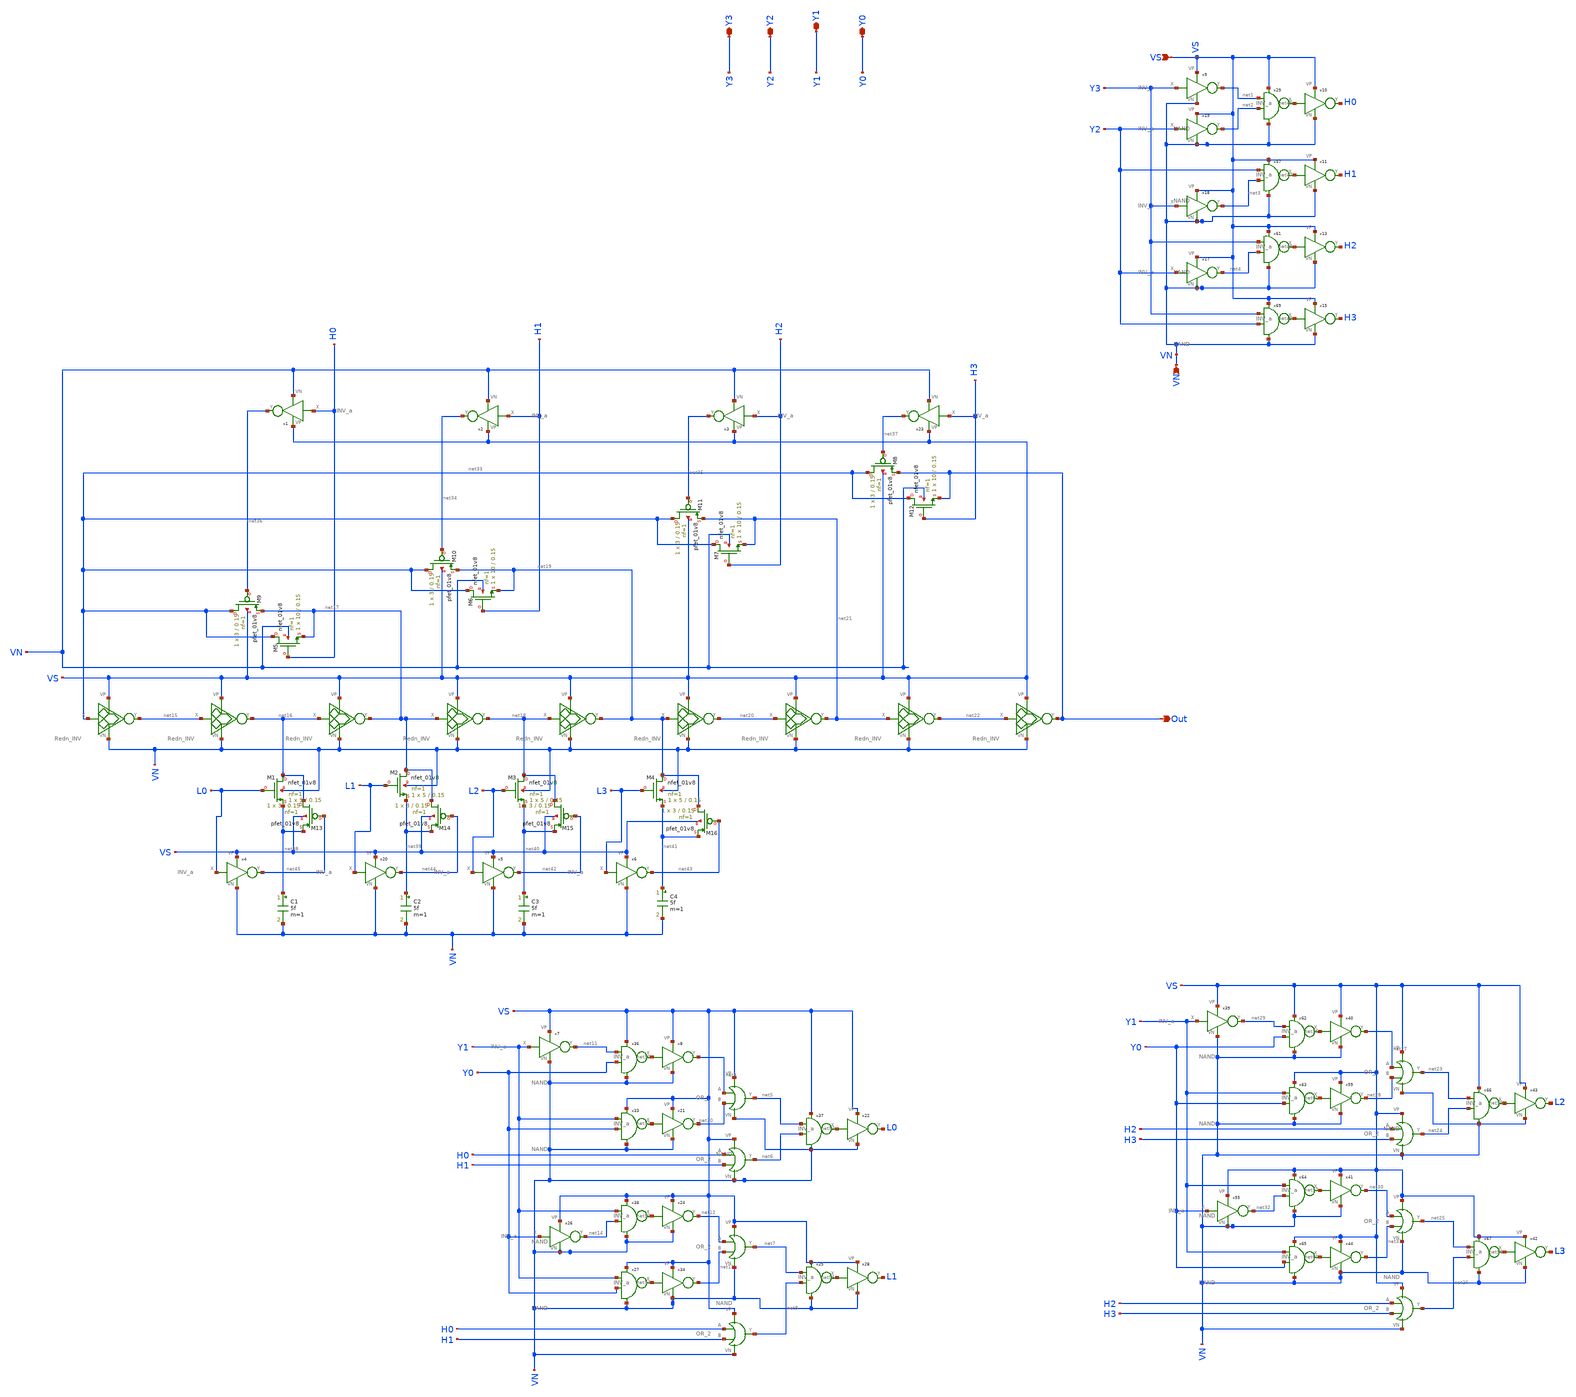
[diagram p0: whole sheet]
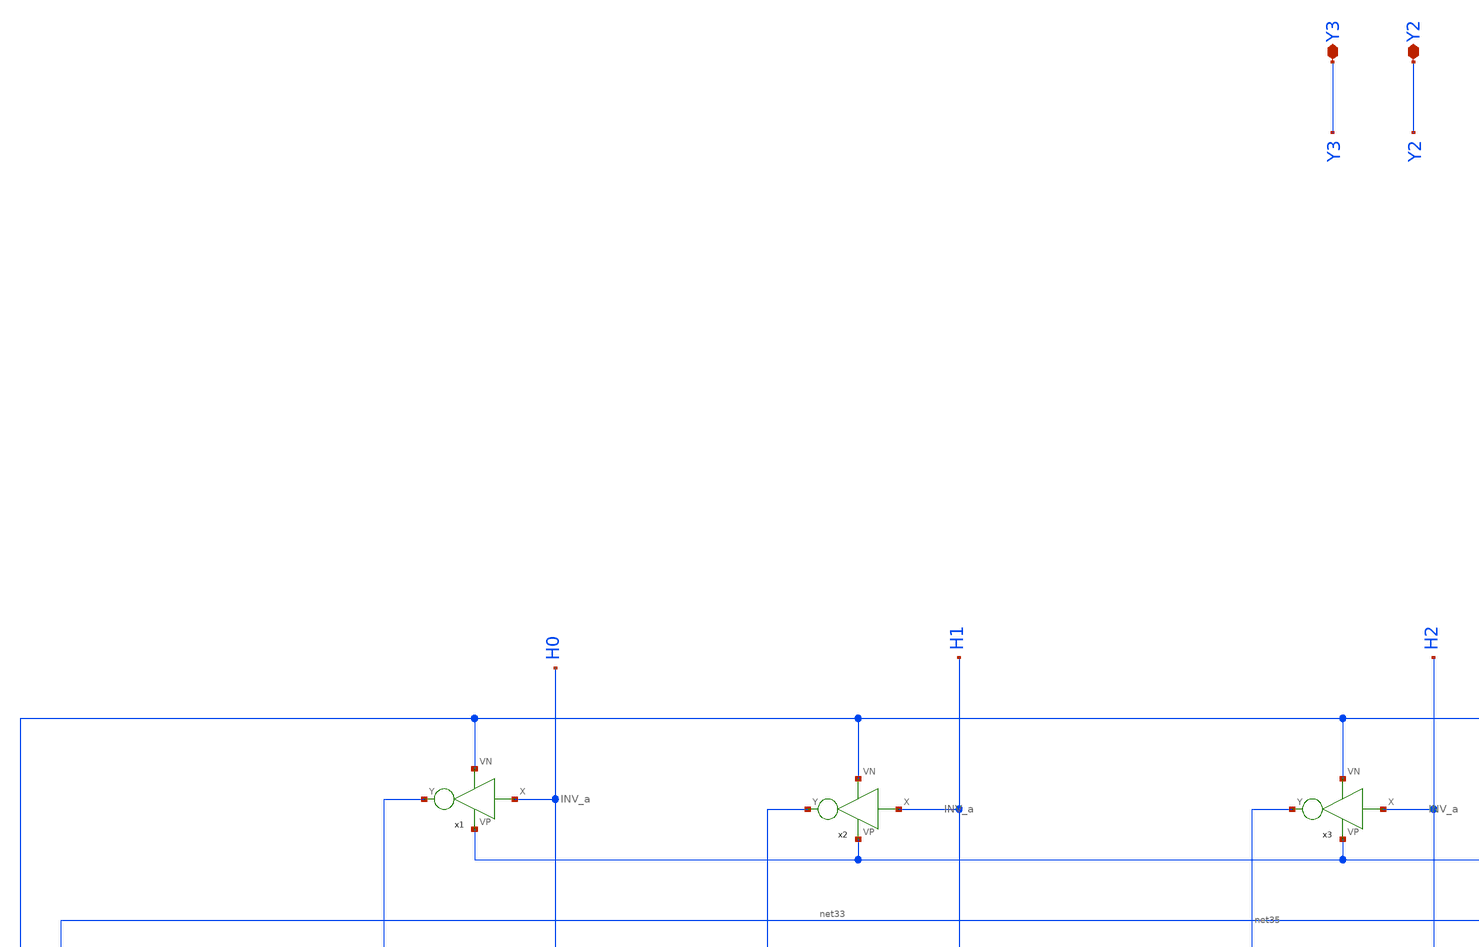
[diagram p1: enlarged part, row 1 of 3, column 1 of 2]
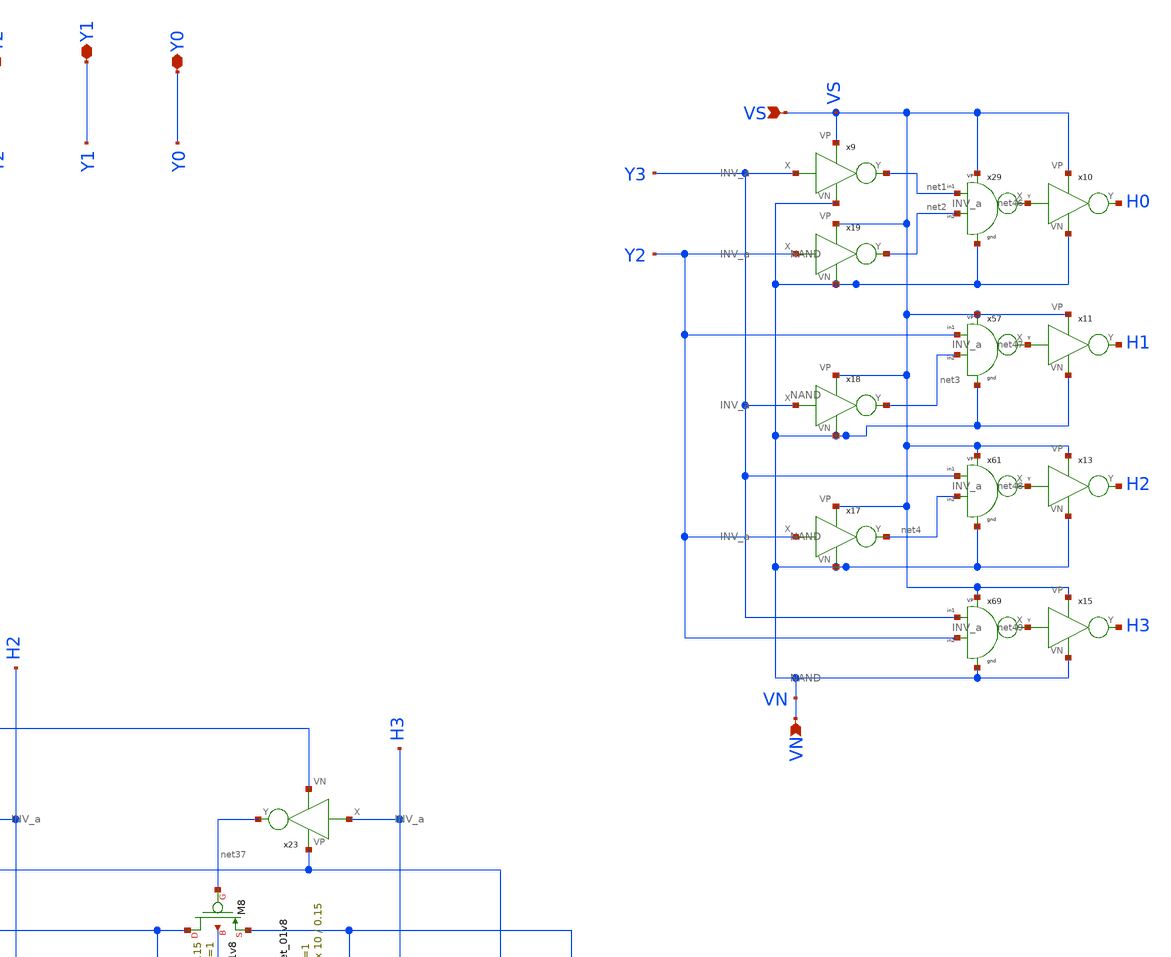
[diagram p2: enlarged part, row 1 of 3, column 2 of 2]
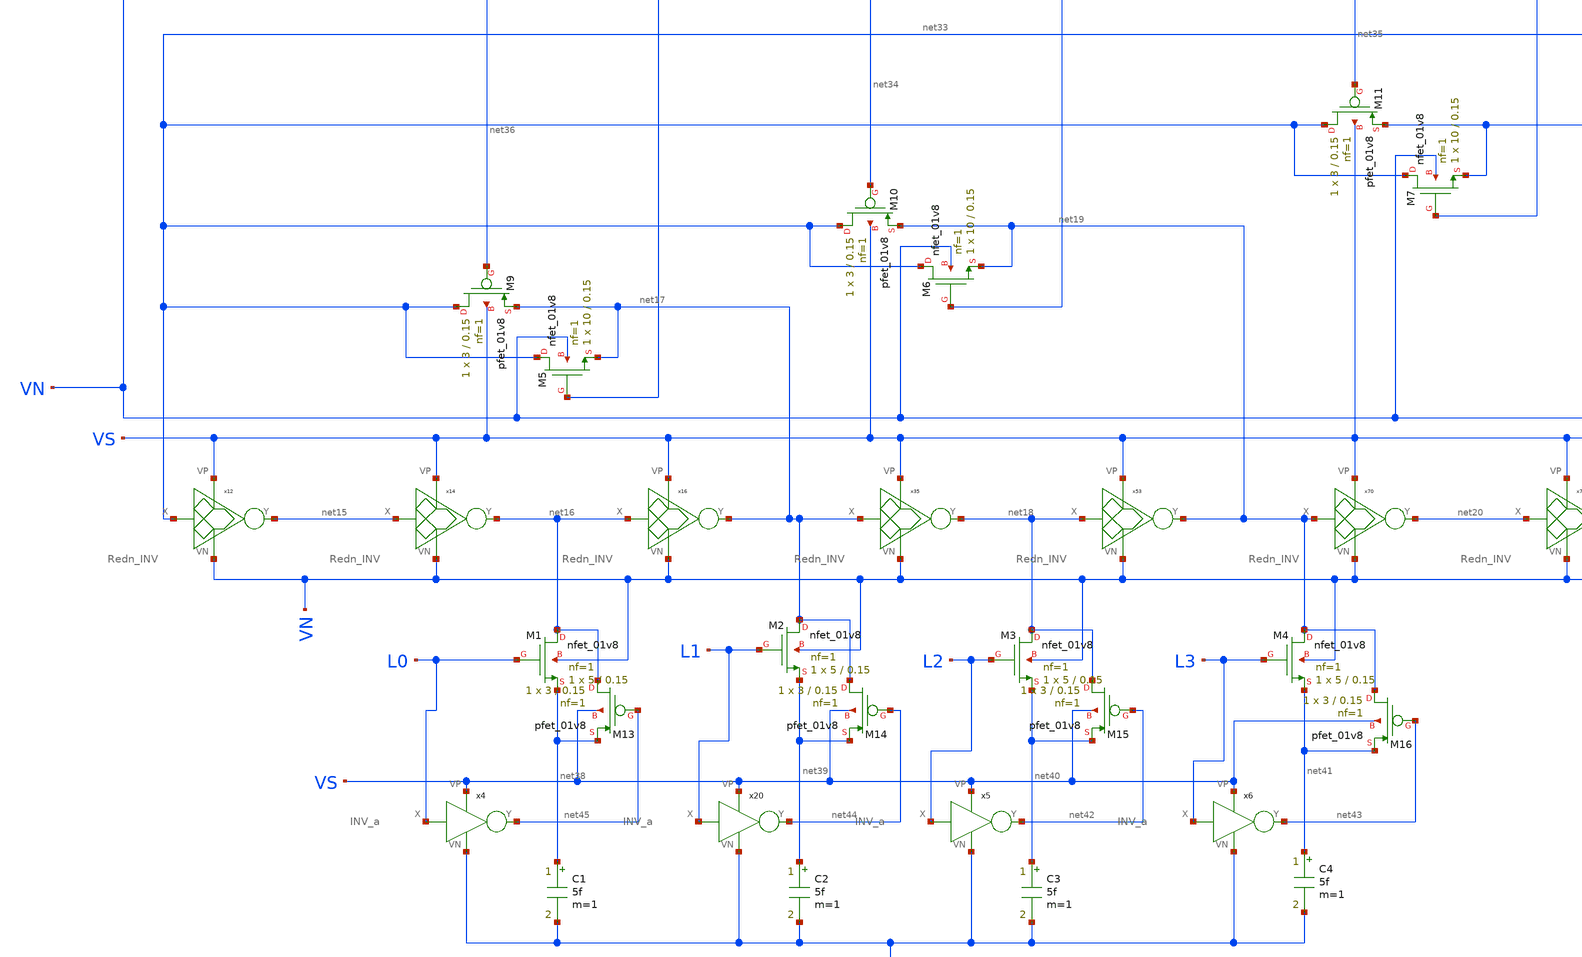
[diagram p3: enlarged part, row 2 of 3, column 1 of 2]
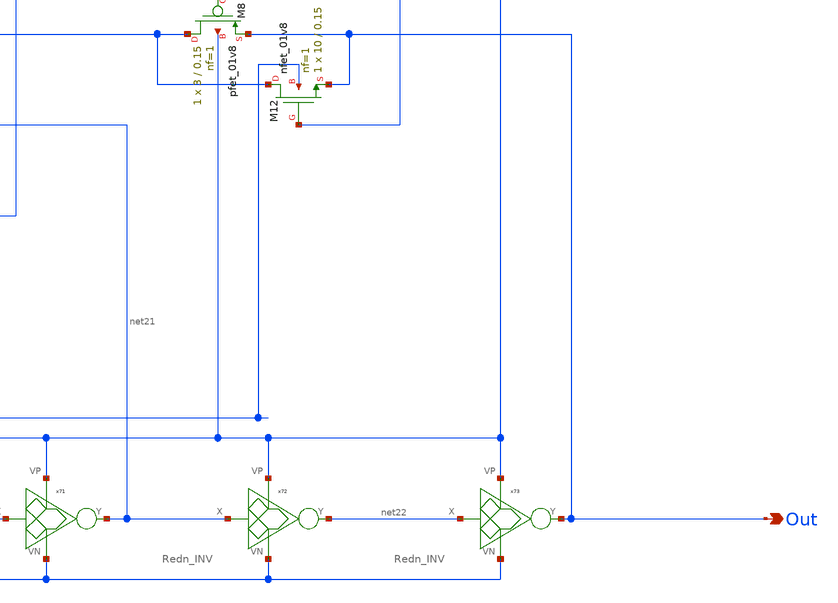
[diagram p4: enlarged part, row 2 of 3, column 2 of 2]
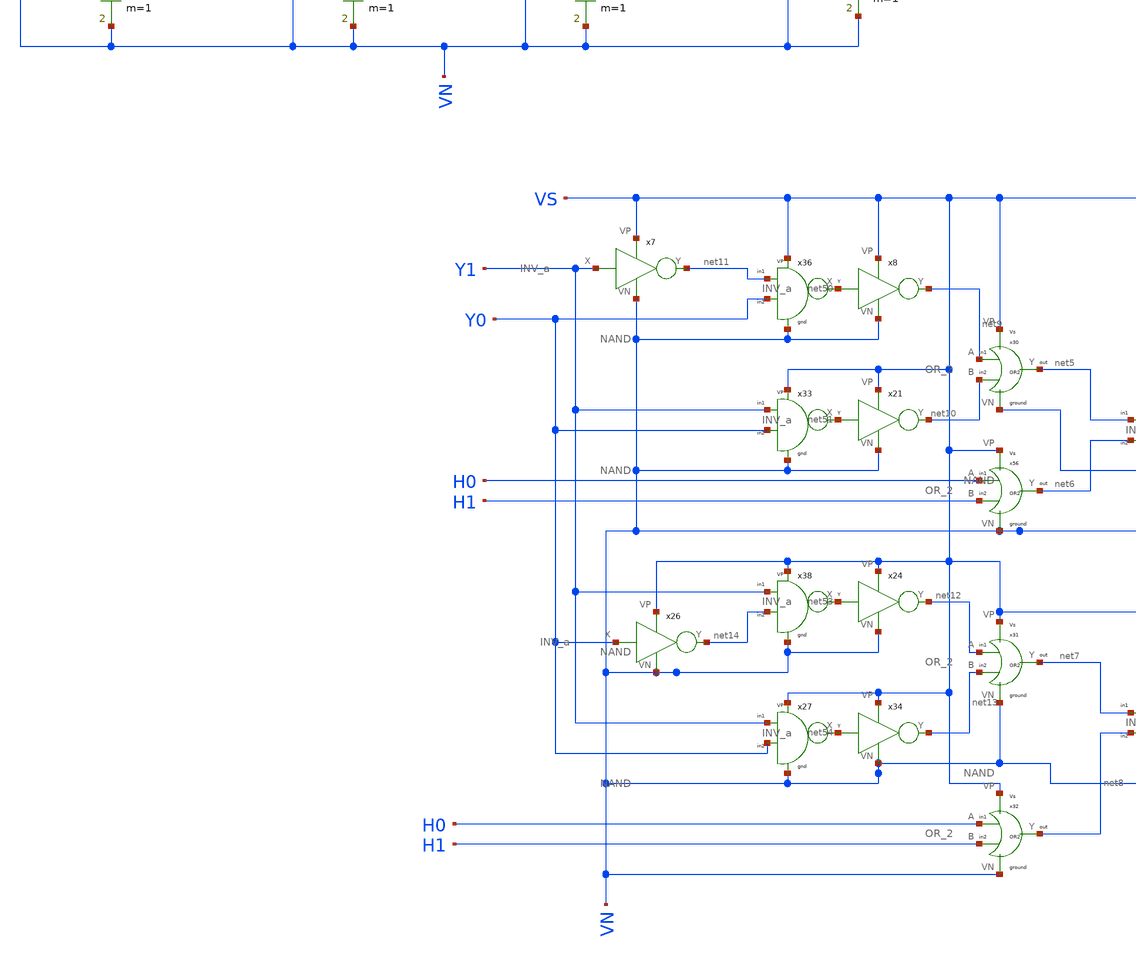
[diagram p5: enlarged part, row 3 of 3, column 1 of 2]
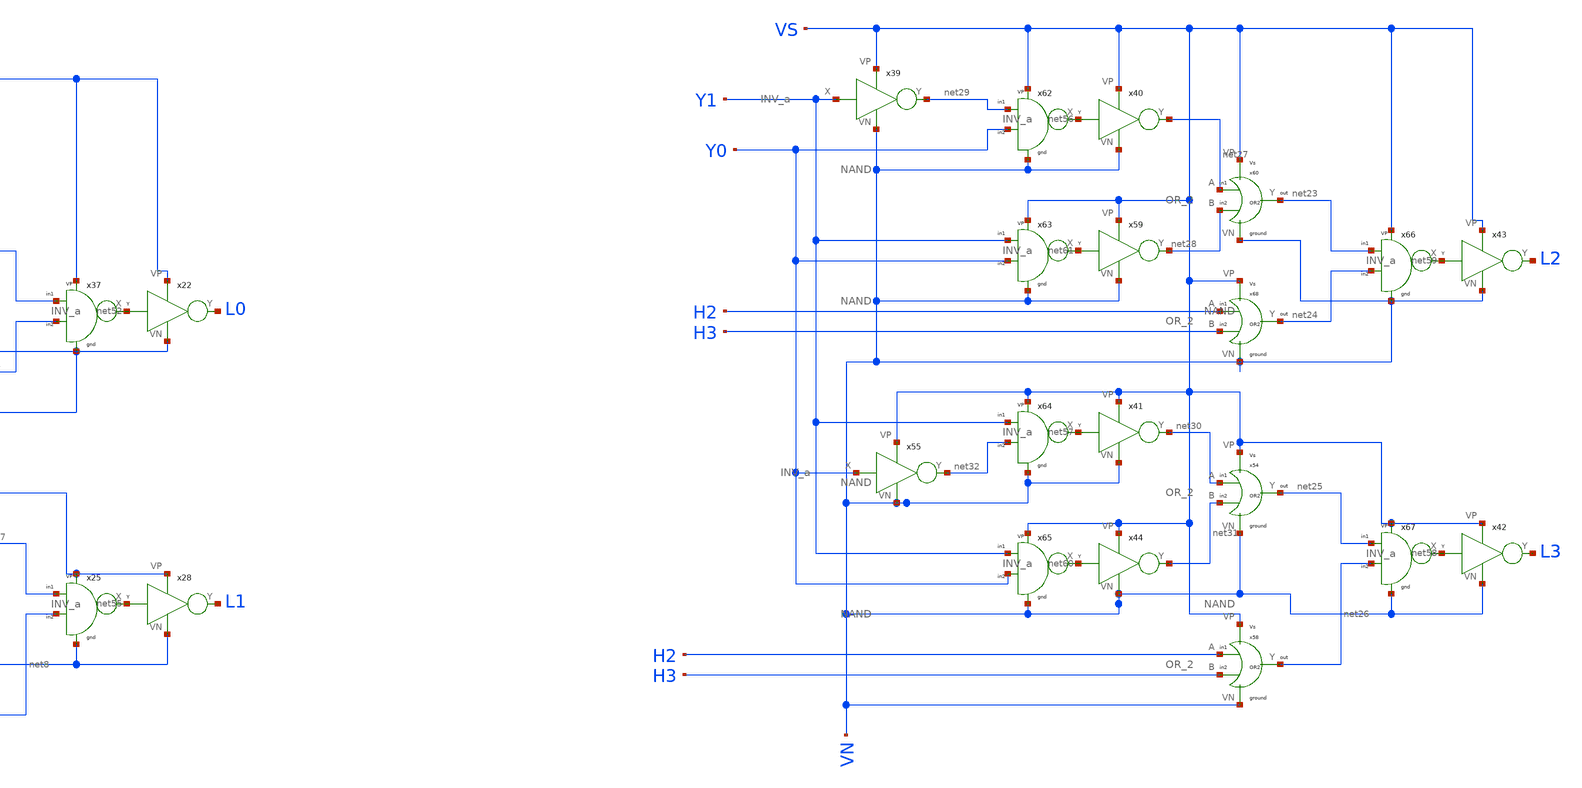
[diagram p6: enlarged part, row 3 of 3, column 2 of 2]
** sch_path: Blocks/DCO/DCO.sch
**.subckt DCO VS Out VN Y3 Y2 Y1 Y0
*.ipin VS
*.opin Out
*.ipin VN
*.iopin Y3
*.iopin Y2
*.iopin Y1
*.iopin Y0
C1 net38 VN 5f m=1
C2 net39 VN 5f m=1
C3 net40 VN 5f m=1
C4 net41 VN 5f m=1
XM1 net16 L0 net38 VN sky130_fd_pr__nfet_01v8 L=0.15 W=5 nf=1 ad='int((nf+1)/2) * W/nf * 0.29' as='int((nf+2)/2) * W/nf * 0.29'
+ pd='2*int((nf+1)/2) * (W/nf + 0.29)' ps='2*int((nf+2)/2) * (W/nf + 0.29)' nrd='0.29 / W' nrs='0.29 / W'
+ sa=0 sb=0 sd=0 mult=1 m=1
XM2 net17 L1 net39 VN sky130_fd_pr__nfet_01v8 L=0.15 W=5 nf=1 ad='int((nf+1)/2) * W/nf * 0.29' as='int((nf+2)/2) * W/nf * 0.29'
+ pd='2*int((nf+1)/2) * (W/nf + 0.29)' ps='2*int((nf+2)/2) * (W/nf + 0.29)' nrd='0.29 / W' nrs='0.29 / W'
+ sa=0 sb=0 sd=0 mult=1 m=1
XM3 net18 L2 net40 VN sky130_fd_pr__nfet_01v8 L=0.15 W=5 nf=1 ad='int((nf+1)/2) * W/nf * 0.29' as='int((nf+2)/2) * W/nf * 0.29'
+ pd='2*int((nf+1)/2) * (W/nf + 0.29)' ps='2*int((nf+2)/2) * (W/nf + 0.29)' nrd='0.29 / W' nrs='0.29 / W'
+ sa=0 sb=0 sd=0 mult=1 m=1
XM4 net19 L3 net41 VN sky130_fd_pr__nfet_01v8 L=0.15 W=5 nf=1 ad='int((nf+1)/2) * W/nf * 0.29' as='int((nf+2)/2) * W/nf * 0.29'
+ pd='2*int((nf+1)/2) * (W/nf + 0.29)' ps='2*int((nf+2)/2) * (W/nf + 0.29)' nrd='0.29 / W' nrs='0.29 / W'
+ sa=0 sb=0 sd=0 mult=1 m=1
XM5 net33 H0 net17 VN sky130_fd_pr__nfet_01v8 L=0.15 W=10 nf=1 ad='int((nf+1)/2) * W/nf * 0.29' as='int((nf+2)/2) * W/nf * 0.29'
+ pd='2*int((nf+1)/2) * (W/nf + 0.29)' ps='2*int((nf+2)/2) * (W/nf + 0.29)' nrd='0.29 / W' nrs='0.29 / W'
+ sa=0 sb=0 sd=0 mult=1 m=1
XM6 net33 H1 net19 VN sky130_fd_pr__nfet_01v8 L=0.15 W=10 nf=1 ad='int((nf+1)/2) * W/nf * 0.29' as='int((nf+2)/2) * W/nf * 0.29'
+ pd='2*int((nf+1)/2) * (W/nf + 0.29)' ps='2*int((nf+2)/2) * (W/nf + 0.29)' nrd='0.29 / W' nrs='0.29 / W'
+ sa=0 sb=0 sd=0 mult=1 m=1
XM7 net33 H2 net21 VN sky130_fd_pr__nfet_01v8 L=0.15 W=10 nf=1 ad='int((nf+1)/2) * W/nf * 0.29' as='int((nf+2)/2) * W/nf * 0.29'
+ pd='2*int((nf+1)/2) * (W/nf + 0.29)' ps='2*int((nf+2)/2) * (W/nf + 0.29)' nrd='0.29 / W' nrs='0.29 / W'
+ sa=0 sb=0 sd=0 mult=1 m=1
XM9 net33 net36 net17 VS sky130_fd_pr__pfet_01v8 L=0.15 W=3 nf=1 ad='int((nf+1)/2) * W/nf * 0.29' as='int((nf+2)/2) * W/nf * 0.29'
+ pd='2*int((nf+1)/2) * (W/nf + 0.29)' ps='2*int((nf+2)/2) * (W/nf + 0.29)' nrd='0.29 / W' nrs='0.29 / W'
+ sa=0 sb=0 sd=0 mult=1 m=1
XM10 net33 net34 net19 VS sky130_fd_pr__pfet_01v8 L=0.15 W=3 nf=1 ad='int((nf+1)/2) * W/nf * 0.29' as='int((nf+2)/2) * W/nf * 0.29'
+ pd='2*int((nf+1)/2) * (W/nf + 0.29)' ps='2*int((nf+2)/2) * (W/nf + 0.29)' nrd='0.29 / W' nrs='0.29 / W'
+ sa=0 sb=0 sd=0 mult=1 m=1
XM11 net33 net35 net21 VS sky130_fd_pr__pfet_01v8 L=0.15 W=3 nf=1 ad='int((nf+1)/2) * W/nf * 0.29' as='int((nf+2)/2) * W/nf * 0.29'
+ pd='2*int((nf+1)/2) * (W/nf + 0.29)' ps='2*int((nf+2)/2) * (W/nf + 0.29)' nrd='0.29 / W' nrs='0.29 / W'
+ sa=0 sb=0 sd=0 mult=1 m=1
XM8 net33 net37 Out VS sky130_fd_pr__pfet_01v8 L=0.15 W=3 nf=1 ad='int((nf+1)/2) * W/nf * 0.29' as='int((nf+2)/2) * W/nf * 0.29'
+ pd='2*int((nf+1)/2) * (W/nf + 0.29)' ps='2*int((nf+2)/2) * (W/nf + 0.29)' nrd='0.29 / W' nrs='0.29 / W'
+ sa=0 sb=0 sd=0 mult=1 m=1
XM12 net33 H3 Out VN sky130_fd_pr__nfet_01v8 L=0.15 W=10 nf=1 ad='int((nf+1)/2) * W/nf * 0.29' as='int((nf+2)/2) * W/nf * 0.29'
+ pd='2*int((nf+1)/2) * (W/nf + 0.29)' ps='2*int((nf+2)/2) * (W/nf + 0.29)' nrd='0.29 / W' nrs='0.29 / W'
+ sa=0 sb=0 sd=0 mult=1 m=1
XM13 net16 net45 net38 VS sky130_fd_pr__pfet_01v8 L=0.15 W=3 nf=1 ad='int((nf+1)/2) * W/nf * 0.29' as='int((nf+2)/2) * W/nf * 0.29'
+ pd='2*int((nf+1)/2) * (W/nf + 0.29)' ps='2*int((nf+2)/2) * (W/nf + 0.29)' nrd='0.29 / W' nrs='0.29 / W'
+ sa=0 sb=0 sd=0 mult=1 m=1
XM14 net17 net44 net39 VS sky130_fd_pr__pfet_01v8 L=0.15 W=3 nf=1 ad='int((nf+1)/2) * W/nf * 0.29' as='int((nf+2)/2) * W/nf * 0.29'
+ pd='2*int((nf+1)/2) * (W/nf + 0.29)' ps='2*int((nf+2)/2) * (W/nf + 0.29)' nrd='0.29 / W' nrs='0.29 / W'
+ sa=0 sb=0 sd=0 mult=1 m=1
XM15 net18 net42 net40 VS sky130_fd_pr__pfet_01v8 L=0.15 W=3 nf=1 ad='int((nf+1)/2) * W/nf * 0.29' as='int((nf+2)/2) * W/nf * 0.29'
+ pd='2*int((nf+1)/2) * (W/nf + 0.29)' ps='2*int((nf+2)/2) * (W/nf + 0.29)' nrd='0.29 / W' nrs='0.29 / W'
+ sa=0 sb=0 sd=0 mult=1 m=1
XM16 net19 net43 net41 VS sky130_fd_pr__pfet_01v8 L=0.15 W=3 nf=1 ad='int((nf+1)/2) * W/nf * 0.29' as='int((nf+2)/2) * W/nf * 0.29'
+ pd='2*int((nf+1)/2) * (W/nf + 0.29)' ps='2*int((nf+2)/2) * (W/nf + 0.29)' nrd='0.29 / W' nrs='0.29 / W'
+ sa=0 sb=0 sd=0 mult=1 m=1
x9 Y3 net1 VS VN INV_a
x10 net46 H0 VS VN INV_a
x11 net47 H1 VS VN INV_a
x13 net48 H2 VS VN INV_a
x15 net49 H3 VS VN INV_a
x17 Y2 net4 VS VN INV_a
x18 Y3 net3 VS VN INV_a
x19 Y2 net2 VS VN INV_a
x23 H3 net37 VS VN INV_a
x3 H2 net35 VS VN INV_a
x2 H1 net34 VS VN INV_a
x1 H0 net36 VS VN INV_a
x4 L0 net45 VS VN INV_a
x20 L1 net44 VS VN INV_a
x5 L2 net42 VS VN INV_a
x6 L3 net43 VS VN INV_a
x7 Y1 net11 VS VN INV_a
x8 net50 net9 VS VN INV_a
x21 net51 net10 VS VN INV_a
x22 net52 L0 VS VN INV_a
x24 net53 net12 VS VN INV_a
x26 Y0 net14 VS VN INV_a
x34 net54 net13 VS VN INV_a
x28 net55 L1 VS VN INV_a
x36 Y0 net11 net50 VS VN NAND
x38 net14 Y1 net53 VS VN NAND
x33 Y0 Y1 net51 VS VN NAND
x37 net6 net5 net52 VS VN NAND
x25 net8 net7 net55 VS VN NAND
x27 Y0 Y1 net54 VS VN NAND
x39 Y1 net29 VS VN INV_a
x40 net56 net27 VS VN INV_a
x41 net57 net30 VS VN INV_a
x42 net58 L3 VS VN INV_a
x43 net59 L2 VS VN INV_a
x44 net60 net31 VS VN INV_a
x55 Y0 net32 VS VN INV_a
x59 net61 net28 VS VN INV_a
x62 Y0 net29 net56 VS VN NAND
x63 Y0 Y1 net61 VS VN NAND
x64 net32 Y1 net57 VS VN NAND
x65 Y0 Y1 net60 VS VN NAND
x66 net24 net23 net59 VS VN NAND
x67 net26 net25 net58 VS VN NAND
x54 net31 net30 net25 VS VN OR_2
x58 H3 H2 net26 VS VN OR_2
x60 net28 net27 net23 VS VN OR_2
x68 H3 H2 net24 VS VN OR_2
x32 H1 H0 net8 VS VN OR_2
x31 net13 net12 net7 VS VN OR_2
x56 H1 H0 net6 VS VN OR_2
x30 net10 net9 net5 VS VN OR_2
x29 net2 net1 net46 VS VN NAND
x57 net3 Y2 net47 VS VN NAND
x61 net4 Y3 net48 VS VN NAND
x69 Y2 Y3 net49 VS VN NAND
x12 net33 net15 VS VN Redn_INV
x14 net15 net16 VS VN Redn_INV
x16 net16 net17 VS VN Redn_INV
x35 net17 net18 VS VN Redn_INV
x53 net18 net19 VS VN Redn_INV
x70 net19 net20 VS VN Redn_INV
x71 net20 net21 VS VN Redn_INV
x72 net21 net22 VS VN Redn_INV
x73 net22 Out VS VN Redn_INV
**.ends

* expanding   symbol:  pico_chipathon/component/INV/INV_a.sym # of pins=4
** sym_path: component/INV/INV_a.sym
** sch_path: component/INV/INV_a.sch
.subckt INV_a X Y VP VN
*.ipin X
*.opin Y
*.iopin VP
*.iopin VN
XM1 Y X VN VN sky130_fd_pr__nfet_01v8 L=0.15 W=1 nf=1 ad='int((nf+1)/2) * W/nf * 0.29' as='int((nf+2)/2) * W/nf * 0.29'
+ pd='2*int((nf+1)/2) * (W/nf + 0.29)' ps='2*int((nf+2)/2) * (W/nf + 0.29)' nrd='0.29 / W' nrs='0.29 / W'
+ sa=0 sb=0 sd=0 mult=1 m=1
XM2 Y X VP VP sky130_fd_pr__pfet_01v8 L=0.15 W=3 nf=1 ad='int((nf+1)/2) * W/nf * 0.29' as='int((nf+2)/2) * W/nf * 0.29'
+ pd='2*int((nf+1)/2) * (W/nf + 0.29)' ps='2*int((nf+2)/2) * (W/nf + 0.29)' nrd='0.29 / W' nrs='0.29 / W'
+ sa=0 sb=0 sd=0 mult=1 m=1
.ends


* expanding   symbol:  pico_chipathon/component/NAND2/NAND.sym # of pins=5
** sym_path: component/NAND2/NAND.sym
** sch_path: component/NAND2/NAND.sch
.subckt NAND B A Y VP VN
*.iopin VP
*.ipin A
*.ipin B
*.opin Y
*.iopin VN
XM1 Y A VP VP sky130_fd_pr__pfet_01v8 L=0.15 W=1.26 nf=1 ad='int((nf+1)/2) * W/nf * 0.29' as='int((nf+2)/2) * W/nf * 0.29'
+ pd='2*int((nf+1)/2) * (W/nf + 0.29)' ps='2*int((nf+2)/2) * (W/nf + 0.29)' nrd='0.29 / W' nrs='0.29 / W'
+ sa=0 sb=0 sd=0 mult=1 m=1
XM2 Y B VP VP sky130_fd_pr__pfet_01v8 L=0.15 W=1.26 nf=1 ad='int((nf+1)/2) * W/nf * 0.29' as='int((nf+2)/2) * W/nf * 0.29'
+ pd='2*int((nf+1)/2) * (W/nf + 0.29)' ps='2*int((nf+2)/2) * (W/nf + 0.29)' nrd='0.29 / W' nrs='0.29 / W'
+ sa=0 sb=0 sd=0 mult=1 m=1
XM3 Y A net1 net1 sky130_fd_pr__nfet_01v8 L=0.15 W=0.84 nf=1 ad='int((nf+1)/2) * W/nf * 0.29' as='int((nf+2)/2) * W/nf * 0.29'
+ pd='2*int((nf+1)/2) * (W/nf + 0.29)' ps='2*int((nf+2)/2) * (W/nf + 0.29)' nrd='0.29 / W' nrs='0.29 / W'
+ sa=0 sb=0 sd=0 mult=1 m=1
XM4 net1 B VN VN sky130_fd_pr__nfet_01v8 L=0.15 W=0.84 nf=1 ad='int((nf+1)/2) * W/nf * 0.29' as='int((nf+2)/2) * W/nf * 0.29'
+ pd='2*int((nf+1)/2) * (W/nf + 0.29)' ps='2*int((nf+2)/2) * (W/nf + 0.29)' nrd='0.29 / W' nrs='0.29 / W'
+ sa=0 sb=0 sd=0 mult=1 m=1
.ends


* expanding   symbol:  pico_chipathon/component/OR2/OR_2.sym # of pins=5
** sym_path: component/OR2/OR_2.sym
** sch_path: component/OR2/OR_2.sch
.subckt OR_2 B A Y VP VN
*.iopin VP
*.iopin VN
*.ipin A
*.ipin B
*.opin Y
XM1 net1 B VN VN sky130_fd_pr__nfet_01v8 L=0.15 W=0.42 nf=1 ad='int((nf+1)/2) * W/nf * 0.29' as='int((nf+2)/2) * W/nf * 0.29'
+ pd='2*int((nf+1)/2) * (W/nf + 0.29)' ps='2*int((nf+2)/2) * (W/nf + 0.29)' nrd='0.29 / W' nrs='0.29 / W'
+ sa=0 sb=0 sd=0 mult=1 m=1
XM2 net1 A VN VN sky130_fd_pr__nfet_01v8 L=0.15 W=0.42 nf=1 ad='int((nf+1)/2) * W/nf * 0.29' as='int((nf+2)/2) * W/nf * 0.29'
+ pd='2*int((nf+1)/2) * (W/nf + 0.29)' ps='2*int((nf+2)/2) * (W/nf + 0.29)' nrd='0.29 / W' nrs='0.29 / W'
+ sa=0 sb=0 sd=0 mult=1 m=1
XM3 net1 B net2 VP sky130_fd_pr__pfet_01v8 L=0.15 W=2.52 nf=1 ad='int((nf+1)/2) * W/nf * 0.29' as='int((nf+2)/2) * W/nf * 0.29'
+ pd='2*int((nf+1)/2) * (W/nf + 0.29)' ps='2*int((nf+2)/2) * (W/nf + 0.29)' nrd='0.29 / W' nrs='0.29 / W'
+ sa=0 sb=0 sd=0 mult=1 m=1
XM4 net2 A VP VP sky130_fd_pr__pfet_01v8 L=0.15 W=2.52 nf=1 ad='int((nf+1)/2) * W/nf * 0.29' as='int((nf+2)/2) * W/nf * 0.29'
+ pd='2*int((nf+1)/2) * (W/nf + 0.29)' ps='2*int((nf+2)/2) * (W/nf + 0.29)' nrd='0.29 / W' nrs='0.29 / W'
+ sa=0 sb=0 sd=0 mult=1 m=1
x1 net1 Y VP VN INV
.ends


* expanding   symbol:  pico_chipathon/component/Reduntant_Inverter/Redn_INV.sym # of pins=4
** sym_path: component/Reduntant_Inverter/Redn_INV.sym
** sch_path: component/Reduntant_Inverter/Redn_INV.sch
.subckt Redn_INV X Y VP VN
*.opin Y
*.ipin X
*.iopin VP
*.iopin VN
XM15 net4 X VN VN sky130_fd_pr__nfet_01v8_lvt L=0.15 W=1 nf=1 ad='int((nf+1)/2) * W/nf * 0.29' as='int((nf+2)/2) * W/nf * 0.29'
+ pd='2*int((nf+1)/2) * (W/nf + 0.29)' ps='2*int((nf+2)/2) * (W/nf + 0.29)' nrd='0.29 / W' nrs='0.29 / W'
+ sa=0 sb=0 sd=0 mult=1 m=1
XM1 net5 X net3 VN sky130_fd_pr__nfet_01v8_lvt L=0.15 W=3.25 nf=1 ad='int((nf+1)/2) * W/nf * 0.29' as='int((nf+2)/2) * W/nf * 0.29'
+ pd='2*int((nf+1)/2) * (W/nf + 0.29)' ps='2*int((nf+2)/2) * (W/nf + 0.29)' nrd='0.29 / W' nrs='0.29 / W'
+ sa=0 sb=0 sd=0 mult=1 m=1
XM16 Y X net6 VN sky130_fd_pr__nfet_01v8_lvt L=0.15 W=6.5 nf=1 ad='int((nf+1)/2) * W/nf * 0.29' as='int((nf+2)/2) * W/nf * 0.29'
+ pd='2*int((nf+1)/2) * (W/nf + 0.29)' ps='2*int((nf+2)/2) * (W/nf + 0.29)' nrd='0.29 / W' nrs='0.29 / W'
+ sa=0 sb=0 sd=0 mult=1 m=1
XM17 net3 X VN VN sky130_fd_pr__nfet_01v8_lvt L=0.15 W=3.25 nf=1 ad='int((nf+1)/2) * W/nf * 0.29' as='int((nf+2)/2) * W/nf * 0.29'
+ pd='2*int((nf+1)/2) * (W/nf + 0.29)' ps='2*int((nf+2)/2) * (W/nf + 0.29)' nrd='0.29 / W' nrs='0.29 / W'
+ sa=0 sb=0 sd=0 mult=1 m=1
XM18 net2 X VN VN sky130_fd_pr__nfet_01v8_lvt L=0.15 W=1.5 nf=1 ad='int((nf+1)/2) * W/nf * 0.29' as='int((nf+2)/2) * W/nf * 0.29'
+ pd='2*int((nf+1)/2) * (W/nf + 0.29)' ps='2*int((nf+2)/2) * (W/nf + 0.29)' nrd='0.29 / W' nrs='0.29 / W'
+ sa=0 sb=0 sd=0 mult=1 m=1
XM19 net1 X VN VN sky130_fd_pr__nfet_01v8_lvt L=0.15 W=6.5 nf=1 ad='int((nf+1)/2) * W/nf * 0.29' as='int((nf+2)/2) * W/nf * 0.29'
+ pd='2*int((nf+1)/2) * (W/nf + 0.29)' ps='2*int((nf+2)/2) * (W/nf + 0.29)' nrd='0.29 / W' nrs='0.29 / W'
+ sa=0 sb=0 sd=0 mult=1 m=1
XM20 net6 X net1 VN sky130_fd_pr__nfet_01v8_lvt L=0.15 W=6.5 nf=1 ad='int((nf+1)/2) * W/nf * 0.29' as='int((nf+2)/2) * W/nf * 0.29'
+ pd='2*int((nf+1)/2) * (W/nf + 0.29)' ps='2*int((nf+2)/2) * (W/nf + 0.29)' nrd='0.29 / W' nrs='0.29 / W'
+ sa=0 sb=0 sd=0 mult=1 m=1
XM2 net4 X VP VP sky130_fd_pr__pfet_01v8 L=0.15 W=10 nf=1 ad='int((nf+1)/2) * W/nf * 0.29' as='int((nf+2)/2) * W/nf * 0.29'
+ pd='2*int((nf+1)/2) * (W/nf + 0.29)' ps='2*int((nf+2)/2) * (W/nf + 0.29)' nrd='0.29 / W' nrs='0.29 / W'
+ sa=0 sb=0 sd=0 mult=1 m=1
XM5 net5 X net4 net4 sky130_fd_pr__pfet_01v8 L=0.15 W=10 nf=1 ad='int((nf+1)/2) * W/nf * 0.29' as='int((nf+2)/2) * W/nf * 0.29'
+ pd='2*int((nf+1)/2) * (W/nf + 0.29)' ps='2*int((nf+2)/2) * (W/nf + 0.29)' nrd='0.29 / W' nrs='0.29 / W'
+ sa=0 sb=0 sd=0 mult=1 m=1
XM6 Y X net5 VP sky130_fd_pr__pfet_01v8 L=0.15 W=10 nf=1 ad='int((nf+1)/2) * W/nf * 0.29' as='int((nf+2)/2) * W/nf * 0.29'
+ pd='2*int((nf+1)/2) * (W/nf + 0.29)' ps='2*int((nf+2)/2) * (W/nf + 0.29)' nrd='0.29 / W' nrs='0.29 / W'
+ sa=0 sb=0 sd=0 mult=1 m=1
XM8 net3 X VP VP sky130_fd_pr__pfet_01v8 L=0.15 W=2 nf=1 ad='int((nf+1)/2) * W/nf * 0.29' as='int((nf+2)/2) * W/nf * 0.29'
+ pd='2*int((nf+1)/2) * (W/nf + 0.29)' ps='2*int((nf+2)/2) * (W/nf + 0.29)' nrd='0.29 / W' nrs='0.29 / W'
+ sa=0 sb=0 sd=0 mult=1 m=1
XM12 net2 X VP VP sky130_fd_pr__pfet_01v8 L=0.15 W=5 nf=1 ad='int((nf+1)/2) * W/nf * 0.29' as='int((nf+2)/2) * W/nf * 0.29'
+ pd='2*int((nf+1)/2) * (W/nf + 0.29)' ps='2*int((nf+2)/2) * (W/nf + 0.29)' nrd='0.29 / W' nrs='0.29 / W'
+ sa=0 sb=0 sd=0 mult=1 m=1
XM14 net6 X net2 VP sky130_fd_pr__pfet_01v8 L=0.15 W=5 nf=1 ad='int((nf+1)/2) * W/nf * 0.29' as='int((nf+2)/2) * W/nf * 0.29'
+ pd='2*int((nf+1)/2) * (W/nf + 0.29)' ps='2*int((nf+2)/2) * (W/nf + 0.29)' nrd='0.29 / W' nrs='0.29 / W'
+ sa=0 sb=0 sd=0 mult=1 m=1
XM21 net1 X VP VP sky130_fd_pr__pfet_01v8 L=0.15 W=1.5 nf=1 ad='int((nf+1)/2) * W/nf * 0.29' as='int((nf+2)/2) * W/nf * 0.29'
+ pd='2*int((nf+1)/2) * (W/nf + 0.29)' ps='2*int((nf+2)/2) * (W/nf + 0.29)' nrd='0.29 / W' nrs='0.29 / W'
+ sa=0 sb=0 sd=0 mult=1 m=1
.ends


* expanding   symbol:  component/Inverter/INV.sym # of pins=4
** sym_path: component/Inverter/INV.sym
** sch_path: component/Inverter/INV.sch
.subckt INV X Y VP VN
*.ipin X
*.opin Y
*.iopin VN
*.iopin VP
XM8 Y X VP VP sky130_fd_pr__pfet_01v8 L=.18 W=1.512 nf=1 ad='int((nf+1)/2) * W/nf * 0.29' as='int((nf+2)/2) * W/nf * 0.29'
+ pd='2*int((nf+1)/2) * (W/nf + 0.29)' ps='2*int((nf+2)/2) * (W/nf + 0.29)' nrd='0.29 / W' nrs='0.29 / W'
+ sa=0 sb=0 sd=0 mult=1 m=1
XM4 Y X VN VN sky130_fd_pr__nfet_01v8 L=0.18 W=0.42 nf=1 ad='int((nf+1)/2) * W/nf * 0.29' as='int((nf+2)/2) * W/nf * 0.29'
+ pd='2*int((nf+1)/2) * (W/nf + 0.29)' ps='2*int((nf+2)/2) * (W/nf + 0.29)' nrd='0.29 / W' nrs='0.29 / W'
+ sa=0 sb=0 sd=0 mult=1 m=1
.ends

.end
